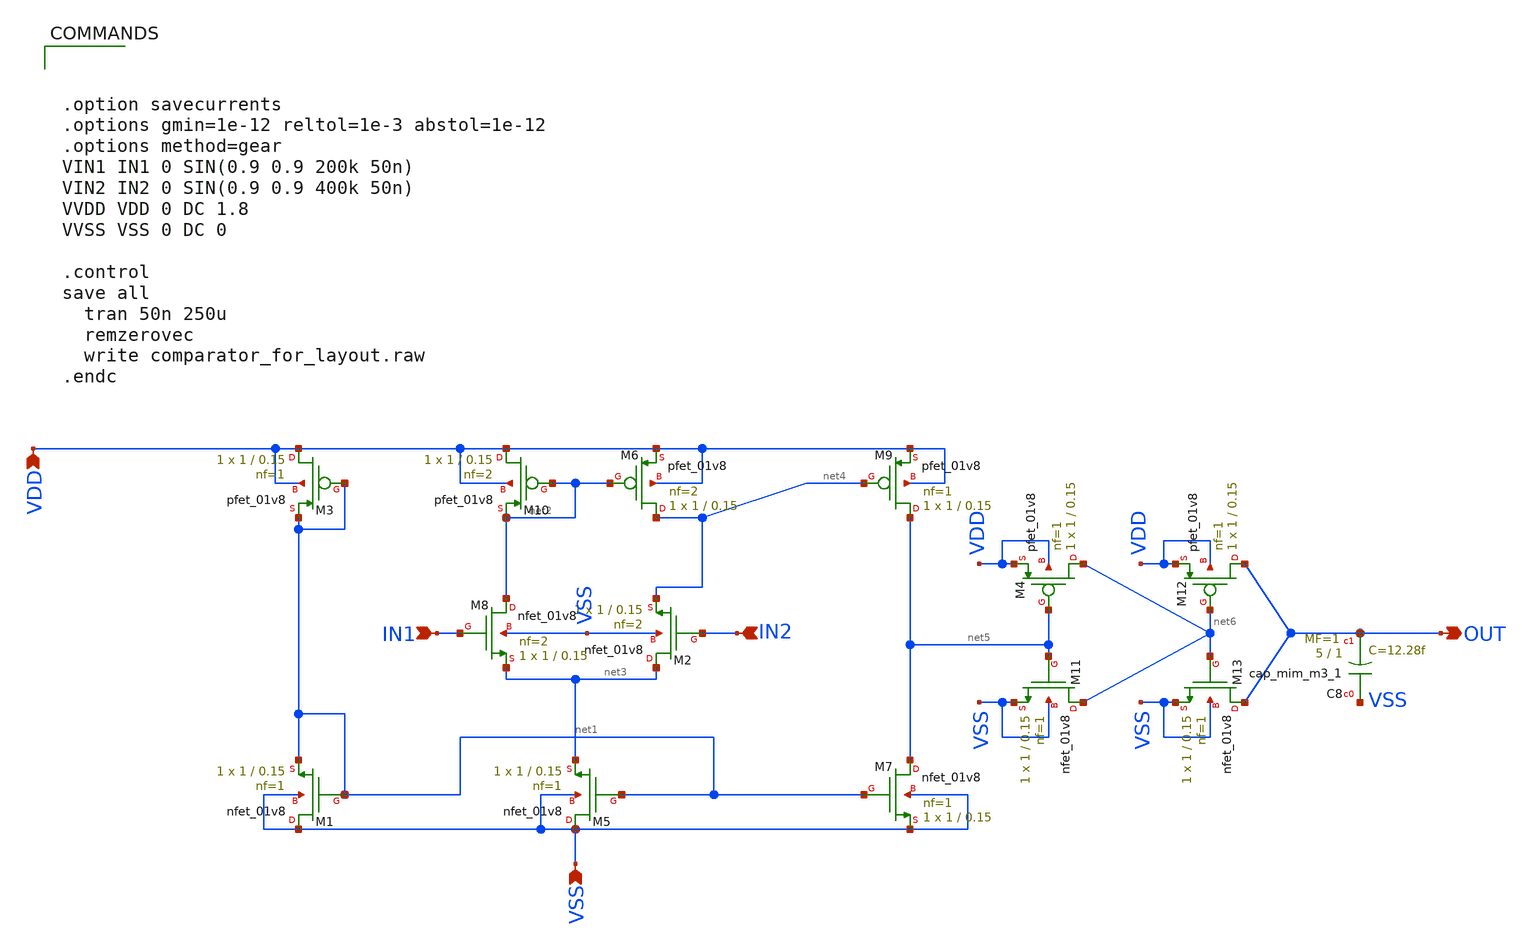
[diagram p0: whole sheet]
** sch_path: comparator_for_layout.sch
**.subckt comparator_for_layout IN1 IN2 OUT VDD VSS
*.ipin IN1
*.ipin IN2
*.opin OUT
*.ipin VDD
*.ipin VSS
XM9 net5 net4 VDD VDD sky130_fd_pr__pfet_01v8 L=0.15 W=1 nf=1 ad='int((nf+1)/2) * W/nf * 0.29' as='int((nf+2)/2) * W/nf * 0.29'
+ pd='2*int((nf+1)/2) * (W/nf + 0.29)' ps='2*int((nf+2)/2) * (W/nf + 0.29)' nrd='0.29 / W' nrs='0.29 / W'
+ sa=0 sb=0 sd=0 mult=1 m=1
XM6 net4 net2 VDD VDD sky130_fd_pr__pfet_01v8 L=0.15 W=1 nf=2 ad='int((nf+1)/2) * W/nf * 0.29' as='int((nf+2)/2) * W/nf * 0.29'
+ pd='2*int((nf+1)/2) * (W/nf + 0.29)' ps='2*int((nf+2)/2) * (W/nf + 0.29)' nrd='0.29 / W' nrs='0.29 / W'
+ sa=0 sb=0 sd=0 mult=1 m=1
XM10 VDD net2 net2 VDD sky130_fd_pr__pfet_01v8 L=0.15 W=1 nf=2 ad='int((nf+1)/2) * W/nf * 0.29' as='int((nf+2)/2) * W/nf * 0.29'
+ pd='2*int((nf+1)/2) * (W/nf + 0.29)' ps='2*int((nf+2)/2) * (W/nf + 0.29)' nrd='0.29 / W' nrs='0.29 / W'
+ sa=0 sb=0 sd=0 mult=1 m=1
XM3 VDD net1 net1 VDD sky130_fd_pr__pfet_01v8 L=0.15 W=1 nf=1 ad='int((nf+1)/2) * W/nf * 0.29' as='int((nf+2)/2) * W/nf * 0.29'
+ pd='2*int((nf+1)/2) * (W/nf + 0.29)' ps='2*int((nf+2)/2) * (W/nf + 0.29)' nrd='0.29 / W' nrs='0.29 / W'
+ sa=0 sb=0 sd=0 mult=1 m=1
XM4 net6 net5 VDD VDD sky130_fd_pr__pfet_01v8 L=0.15 W=1 nf=1 ad='int((nf+1)/2) * W/nf * 0.29' as='int((nf+2)/2) * W/nf * 0.29'
+ pd='2*int((nf+1)/2) * (W/nf + 0.29)' ps='2*int((nf+2)/2) * (W/nf + 0.29)' nrd='0.29 / W' nrs='0.29 / W'
+ sa=0 sb=0 sd=0 mult=1 m=1
XM12 OUT net6 VDD VDD sky130_fd_pr__pfet_01v8 L=0.15 W=1 nf=1 ad='int((nf+1)/2) * W/nf * 0.29' as='int((nf+2)/2) * W/nf * 0.29'
+ pd='2*int((nf+1)/2) * (W/nf + 0.29)' ps='2*int((nf+2)/2) * (W/nf + 0.29)' nrd='0.29 / W' nrs='0.29 / W'
+ sa=0 sb=0 sd=0 mult=1 m=1
XM2 net3 IN2 net4 VSS sky130_fd_pr__nfet_01v8 L=0.15 W=1 nf=2 ad='int((nf+1)/2) * W/nf * 0.29' as='int((nf+2)/2) * W/nf * 0.29'
+ pd='2*int((nf+1)/2) * (W/nf + 0.29)' ps='2*int((nf+2)/2) * (W/nf + 0.29)' nrd='0.29 / W' nrs='0.29 / W'
+ sa=0 sb=0 sd=0 mult=1 m=1
XM1 VSS net1 net1 VSS sky130_fd_pr__nfet_01v8 L=0.15 W=1 nf=1 ad='int((nf+1)/2) * W/nf * 0.29' as='int((nf+2)/2) * W/nf * 0.29'
+ pd='2*int((nf+1)/2) * (W/nf + 0.29)' ps='2*int((nf+2)/2) * (W/nf + 0.29)' nrd='0.29 / W' nrs='0.29 / W'
+ sa=0 sb=0 sd=0 mult=1 m=1
XM5 VSS net1 net3 VSS sky130_fd_pr__nfet_01v8 L=0.15 W=1 nf=1 ad='int((nf+1)/2) * W/nf * 0.29' as='int((nf+2)/2) * W/nf * 0.29'
+ pd='2*int((nf+1)/2) * (W/nf + 0.29)' ps='2*int((nf+2)/2) * (W/nf + 0.29)' nrd='0.29 / W' nrs='0.29 / W'
+ sa=0 sb=0 sd=0 mult=1 m=1
XM7 net5 net1 VSS VSS sky130_fd_pr__nfet_01v8 L=0.15 W=1 nf=1 ad='int((nf+1)/2) * W/nf * 0.29' as='int((nf+2)/2) * W/nf * 0.29'
+ pd='2*int((nf+1)/2) * (W/nf + 0.29)' ps='2*int((nf+2)/2) * (W/nf + 0.29)' nrd='0.29 / W' nrs='0.29 / W'
+ sa=0 sb=0 sd=0 mult=1 m=1
XM8 net2 IN1 net3 VSS sky130_fd_pr__nfet_01v8 L=0.15 W=1 nf=2 ad='int((nf+1)/2) * W/nf * 0.29' as='int((nf+2)/2) * W/nf * 0.29'
+ pd='2*int((nf+1)/2) * (W/nf + 0.29)' ps='2*int((nf+2)/2) * (W/nf + 0.29)' nrd='0.29 / W' nrs='0.29 / W'
+ sa=0 sb=0 sd=0 mult=1 m=1
XM11 net6 net5 VSS VSS sky130_fd_pr__nfet_01v8 L=0.15 W=1 nf=1 ad='int((nf+1)/2) * W/nf * 0.29' as='int((nf+2)/2) * W/nf * 0.29'
+ pd='2*int((nf+1)/2) * (W/nf + 0.29)' ps='2*int((nf+2)/2) * (W/nf + 0.29)' nrd='0.29 / W' nrs='0.29 / W'
+ sa=0 sb=0 sd=0 mult=1 m=1
XM13 OUT net6 VSS VSS sky130_fd_pr__nfet_01v8 L=0.15 W=1 nf=1 ad='int((nf+1)/2) * W/nf * 0.29' as='int((nf+2)/2) * W/nf * 0.29'
+ pd='2*int((nf+1)/2) * (W/nf + 0.29)' ps='2*int((nf+2)/2) * (W/nf + 0.29)' nrd='0.29 / W' nrs='0.29 / W'
+ sa=0 sb=0 sd=0 mult=1 m=1
XC8 VSS OUT sky130_fd_pr__cap_mim_m3_1 W=5 L=1 MF=1 m=1
**** begin user architecture code

** opencircuitdesign pdks install
.lib $::SKYWATER_MODELS/sky130.lib.spice tt
.include $::SKYWATER_STDCELLS/sky130_fd_sc_hd.spice
.include /foss/pdks/sky130A/libs.tech/xschem/sky130_stdcells/




.option savecurrents
.options gmin=1e-12 reltol=1e-3 abstol=1e-12
.options method=gear
VIN1 IN1 0 SIN(0.9 0.9 200k 50n)
VIN2 IN2 0 SIN(0.9 0.9 400k 50n)
VVDD VDD 0 DC 1.8
VVSS VSS 0 DC 0

.control
save all
  tran 50n 250u
  remzerovec
  write comparator_for_layout.raw
.endc


**** end user architecture code
**.ends
.end
